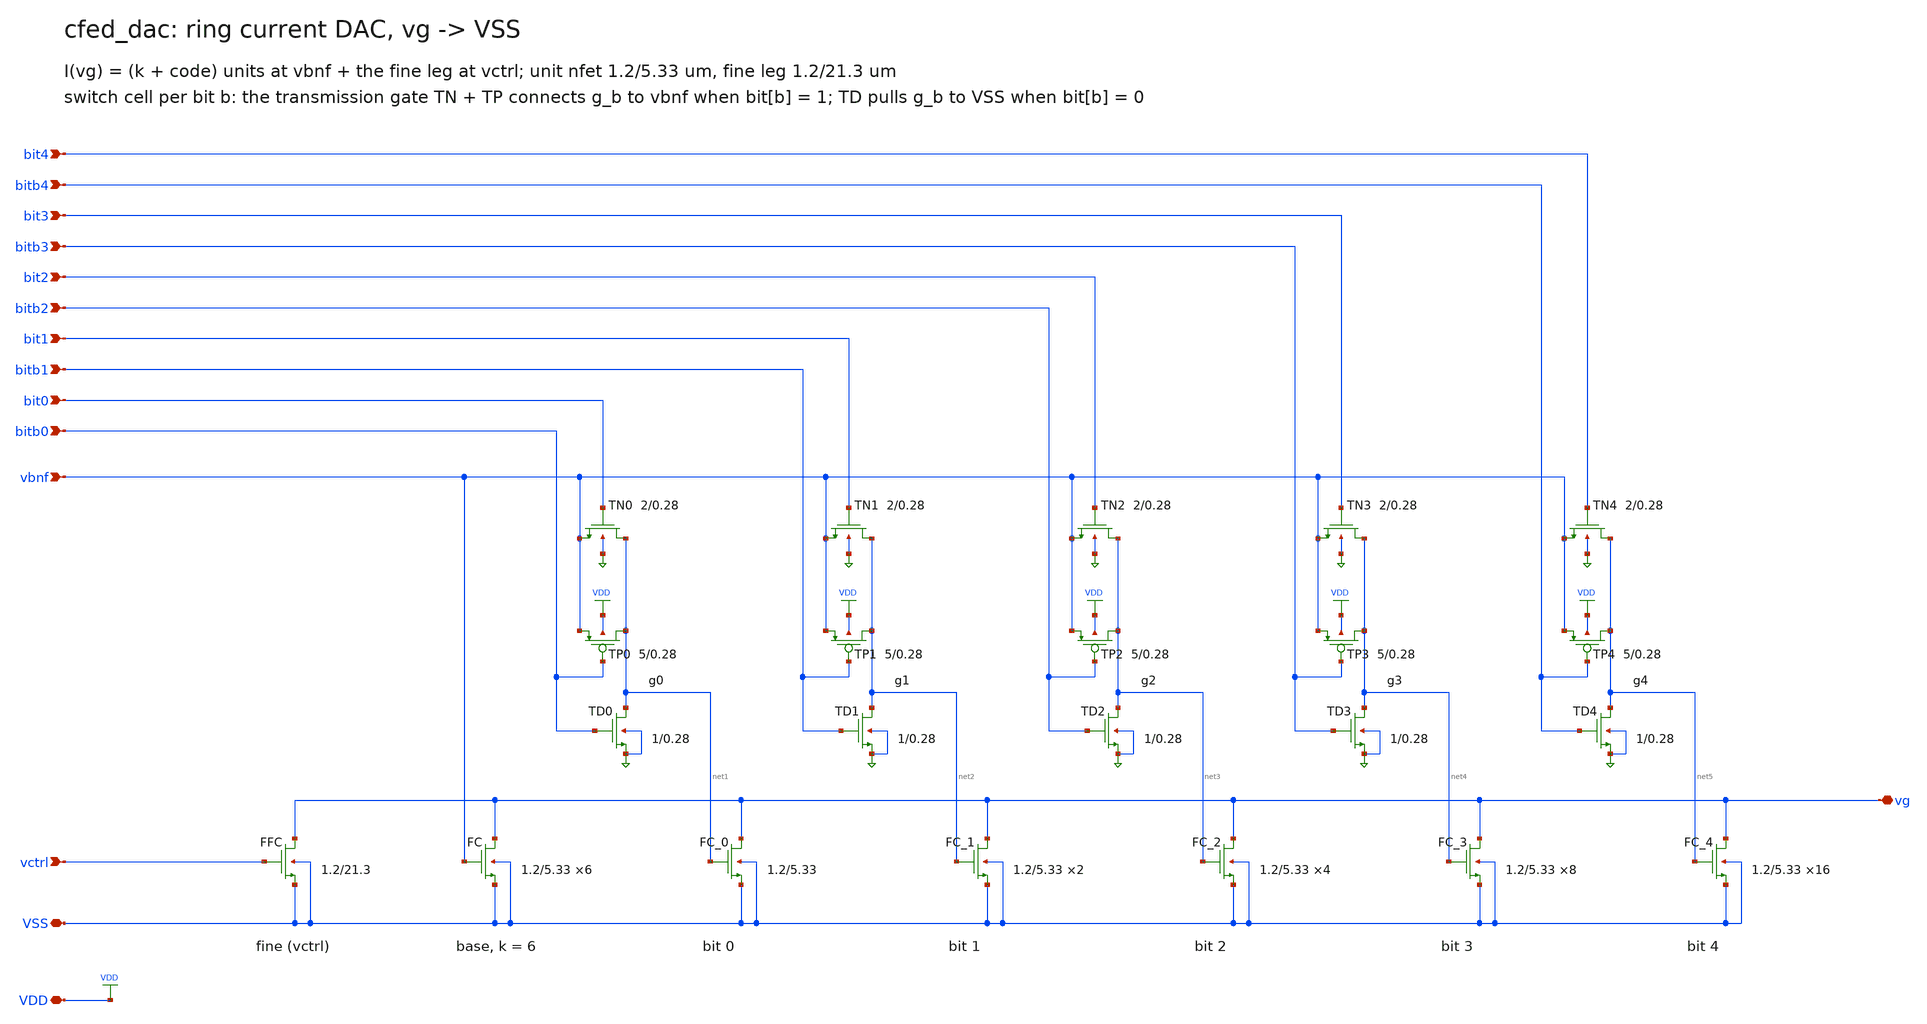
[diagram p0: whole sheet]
** sch_path: xschem/cfed_dac.sch
**.subckt cfed_dac vg vbnf vctrl bit0 bit1 bit2 bit3 bit4 bitb0 bitb1 bitb2 bitb3 bitb4 VDD VSS
*.iopin vg
*.ipin vbnf
*.ipin vctrl
*.ipin bit0
*.ipin bit1
*.ipin bit2
*.ipin bit3
*.ipin bit4
*.ipin bitb0
*.ipin bitb1
*.ipin bitb2
*.ipin bitb3
*.ipin bitb4
*.iopin VDD
*.iopin VSS
XFFC vg vctrl VSS VSS nfet_03v3 L=21.333333333333332u W=1.2u nf=1 ad=0.6p as=0.6p pd=3.4u ps=3.4u
+ nrd=0 nrs=0 sa=0 sb=0 sd=0 m=1
XFC vg vbnf VSS VSS nfet_03v3 L=5.333333333333333u W=1.2u nf=1 ad=0.6p as=0.6p pd=3.4u ps=3.4u nrd=0
+ nrs=0 sa=0 sb=0 sd=0 m=6
XFC_0 vg net1 VSS VSS nfet_03v3 L=5.333333333333333u W=1.2u nf=1 ad=0.6p as=0.6p pd=3.4u ps=3.4u
+ nrd=0 nrs=0 sa=0 sb=0 sd=0 m=1
XFC_1 vg net2 VSS VSS nfet_03v3 L=5.333333333333333u W=1.2u nf=1 ad=0.6p as=0.6p pd=3.4u ps=3.4u
+ nrd=0 nrs=0 sa=0 sb=0 sd=0 m=2
XFC_2 vg net3 VSS VSS nfet_03v3 L=5.333333333333333u W=1.2u nf=1 ad=0.6p as=0.6p pd=3.4u ps=3.4u
+ nrd=0 nrs=0 sa=0 sb=0 sd=0 m=4
XFC_3 vg net4 VSS VSS nfet_03v3 L=5.333333333333333u W=1.2u nf=1 ad=0.6p as=0.6p pd=3.4u ps=3.4u
+ nrd=0 nrs=0 sa=0 sb=0 sd=0 m=8
XFC_4 vg net5 VSS VSS nfet_03v3 L=5.333333333333333u W=1.2u nf=1 ad=0.6p as=0.6p pd=3.4u ps=3.4u
+ nrd=0 nrs=0 sa=0 sb=0 sd=0 m=16
XTN0 net1 bit0 vbnf VSS nfet_03v3 L=0.28u W=2.0u nf=1 ad=1.0p as=1.0p pd=5.0u ps=5.0u nrd=0 nrs=0
+ sa=0 sb=0 sd=0 m=1
XTP0 net1 bitb0 vbnf VDD pfet_03v3 L=0.28u W=5.0u nf=1 ad=2.5p as=2.5p pd=11.0u ps=11.0u nrd=0 nrs=0
+ sa=0 sb=0 sd=0 m=1
XTD0 net1 bitb0 VSS VSS nfet_03v3 L=0.28u W=1.0u nf=1 ad=0.5p as=0.5p pd=3.0u ps=3.0u nrd=0 nrs=0
+ sa=0 sb=0 sd=0 m=1
XTN1 net2 bit1 vbnf VSS nfet_03v3 L=0.28u W=2.0u nf=1 ad=1.0p as=1.0p pd=5.0u ps=5.0u nrd=0 nrs=0
+ sa=0 sb=0 sd=0 m=1
XTP1 net2 bitb1 vbnf VDD pfet_03v3 L=0.28u W=5.0u nf=1 ad=2.5p as=2.5p pd=11.0u ps=11.0u nrd=0 nrs=0
+ sa=0 sb=0 sd=0 m=1
XTD1 net2 bitb1 VSS VSS nfet_03v3 L=0.28u W=1.0u nf=1 ad=0.5p as=0.5p pd=3.0u ps=3.0u nrd=0 nrs=0
+ sa=0 sb=0 sd=0 m=1
XTN2 net3 bit2 vbnf VSS nfet_03v3 L=0.28u W=2.0u nf=1 ad=1.0p as=1.0p pd=5.0u ps=5.0u nrd=0 nrs=0
+ sa=0 sb=0 sd=0 m=1
XTP2 net3 bitb2 vbnf VDD pfet_03v3 L=0.28u W=5.0u nf=1 ad=2.5p as=2.5p pd=11.0u ps=11.0u nrd=0 nrs=0
+ sa=0 sb=0 sd=0 m=1
XTD2 net3 bitb2 VSS VSS nfet_03v3 L=0.28u W=1.0u nf=1 ad=0.5p as=0.5p pd=3.0u ps=3.0u nrd=0 nrs=0
+ sa=0 sb=0 sd=0 m=1
XTN3 net4 bit3 vbnf VSS nfet_03v3 L=0.28u W=2.0u nf=1 ad=1.0p as=1.0p pd=5.0u ps=5.0u nrd=0 nrs=0
+ sa=0 sb=0 sd=0 m=1
XTP3 net4 bitb3 vbnf VDD pfet_03v3 L=0.28u W=5.0u nf=1 ad=2.5p as=2.5p pd=11.0u ps=11.0u nrd=0 nrs=0
+ sa=0 sb=0 sd=0 m=1
XTD3 net4 bitb3 VSS VSS nfet_03v3 L=0.28u W=1.0u nf=1 ad=0.5p as=0.5p pd=3.0u ps=3.0u nrd=0 nrs=0
+ sa=0 sb=0 sd=0 m=1
XTN4 net5 bit4 vbnf VSS nfet_03v3 L=0.28u W=2.0u nf=1 ad=1.0p as=1.0p pd=5.0u ps=5.0u nrd=0 nrs=0
+ sa=0 sb=0 sd=0 m=1
XTP4 net5 bitb4 vbnf VDD pfet_03v3 L=0.28u W=5.0u nf=1 ad=2.5p as=2.5p pd=11.0u ps=11.0u nrd=0 nrs=0
+ sa=0 sb=0 sd=0 m=1
XTD4 net5 bitb4 VSS VSS nfet_03v3 L=0.28u W=1.0u nf=1 ad=0.5p as=0.5p pd=3.0u ps=3.0u nrd=0 nrs=0
+ sa=0 sb=0 sd=0 m=1
**.ends
.end
